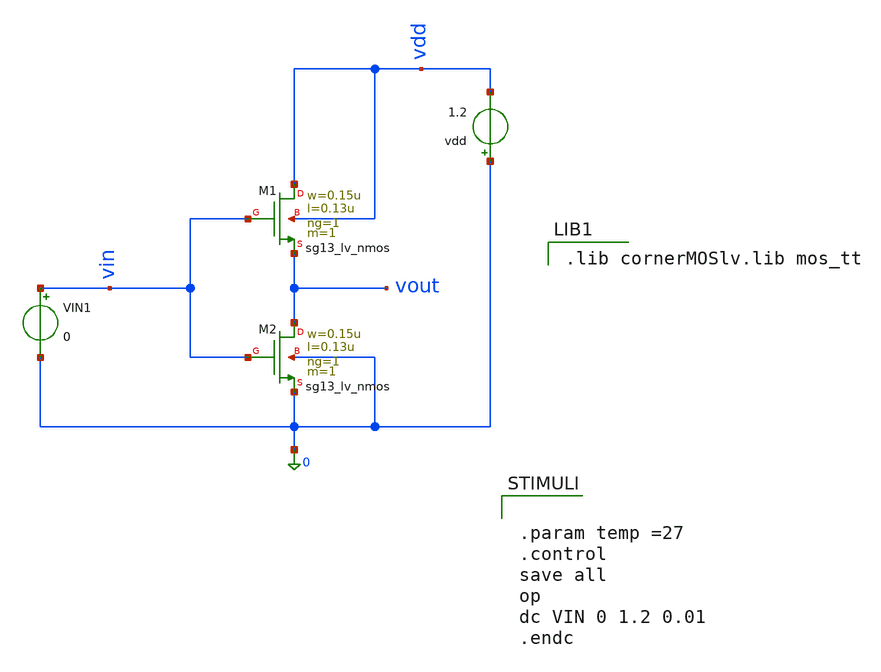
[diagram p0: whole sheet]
** sch_path: untitled.sch
**.subckt untitled
XM1 vdd vin vout vdd sg13_lv_nmos w=0.15u l=0.13u ng=1 m=1 mm_ok=1
vdd 0 vdd 1.2
VIN1 vin 0 0
XM2 vout vin 0 0 sg13_lv_nmos w=0.15u l=0.13u ng=1 m=1 mm_ok=1
**** begin user architecture code

.lib cornerMOSlv.lib mos_tt



.param temp =27
.control
save all
op
dc VIN 0 1.2 0.01
.endc


**** end user architecture code
**.ends
.end
